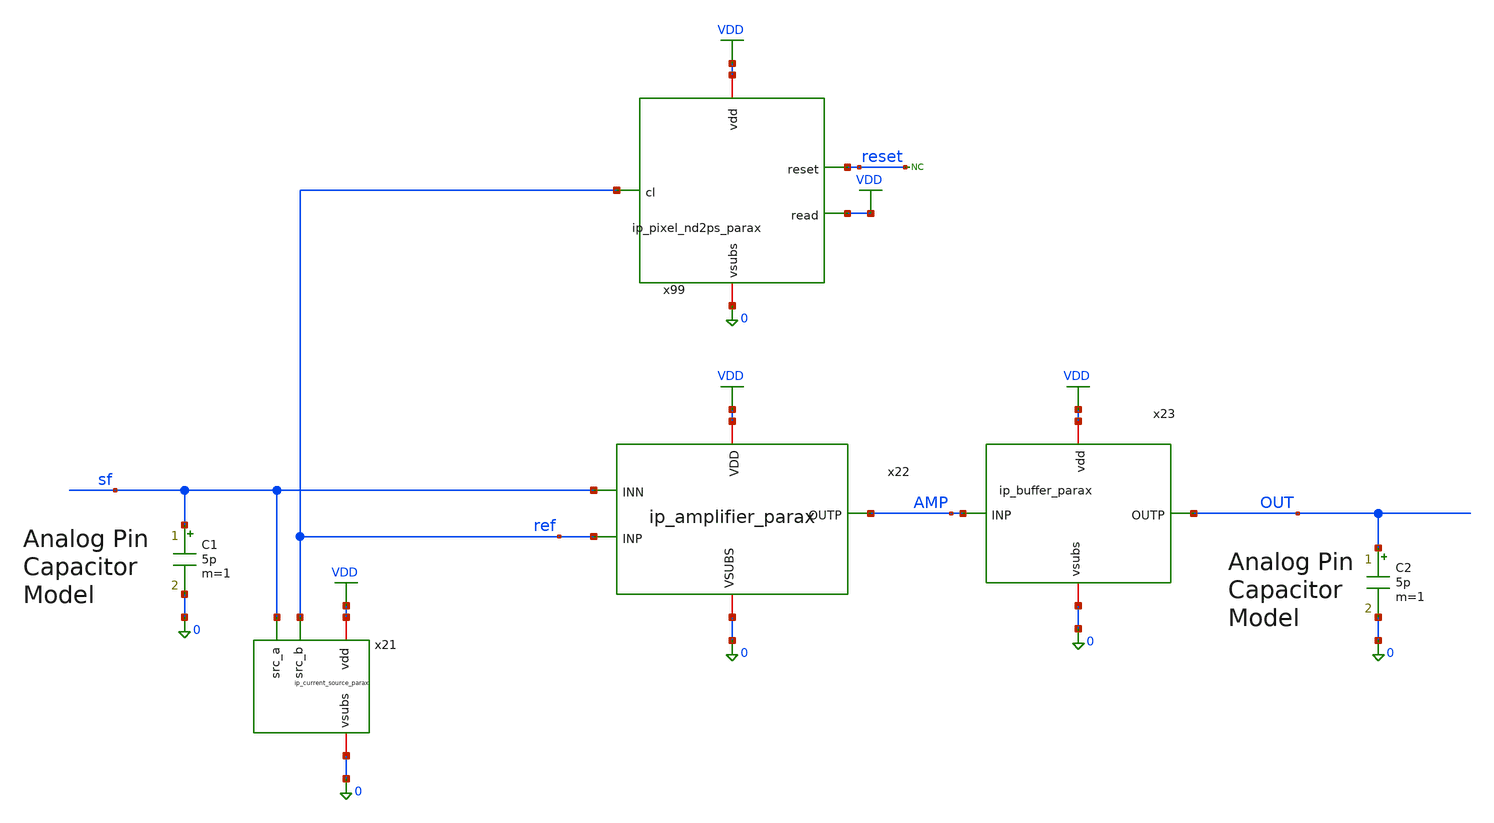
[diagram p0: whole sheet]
** sch_path: xschem/tb_total_tran.sch
**.subckt tb_total_tran
x21 VDD sf 0 ref ip_current_source_parax
x22 VDD AMP ref sf 0 ip_amplifier_parax
x99 VDD reset VDD 0 ref ip_pixel_nd2ps_parax
C1 sf 0 5p m=1
x23 VDD OUT AMP 0 ip_buffer_parax
C2 OUT 0 5p m=1
* noconn reset
**** begin user architecture code

.include $::180MCU_MODELS/design.ngspice
.lib $::180MCU_MODELS/sm141064.ngspice typical
.lib $::180MCU_MODELS/sm141064.ngspice res_typical
.lib $::180MCU_MODELS/sm141064.ngspice moscap_typical
.lib $::180MCU_MODELS/sm141064.ngspice diode_typical




.control
	reset
	tran 1u 1.8m
	save all
	write tb_total_tran.raw
	quit
.endc





VVDD VDD 0 3.3
VCLK CLK 0 PULSE (0 3.3 5u 1n 1n 5u 10u)

astim [RESETA        nRA4 nRA3 nRA2 nRA1 nRA0        nCA4 nCA3 nCA2 nCA1 nCA0] stim
.model stim d_source input_file="../st_total.txt"

acosim[CLK        nCA4 nCA3 nCA2 nCA1 nCA0        nRA4 nRA3 nRA2 nRA1 nRA0        RESETA]
+        [reset        nCY20 nCY19 nCY18 nCY17 nCY16 nCY15        nCY14 nCY13 nCY12 nCY11 nCY10 nCY9         nCY8
+  nCY7  nCY6  nCY5  nCY4  nCY3         nCY2  nCY1  nCY0         nRY16 nRY15 nRY14 nRY13 nRY12 nRY11
+         nRY10 nRY9  nRY8  nRY7  nRY6  nRY5        nRY4  nRY3  nRY2  nRY1  nRY0        ] null dut
.model dut d_cosim simulation="../../verilog/rtl/aux_total_digital/aux_total_digital.so"

RnRA0  nRA0 0 100k
RnRA1  nRA1 0 100k
RnRA2  nRA2 0 100k
RnRA3  nRA3 0 100k
RnRA4  nRA4 0 100k

RnCA0  nCA0 0 100k
RnCA1  nCA1 0 100k
RnCA2  nCA2 0 100k
RnCA3  nCA3 0 100k
RnCA4  nCA4 0 100k

RnRY7  nRY7 0 100k
RnRY6  nRY6 0 100k
RnRY5  nRY5 0 100k
RnRY4  nRY4 0 100k
RnRY3  nRY3 0 100k
RnRY2  nRY2 0 100k
RnRY1  nRY1 0 100k
RnRY0  nRY0 0 100k

RnCY5  nCY5 0 100k
RnCY4  nCY4 0 100k
RnCY3  nCY3 0 100k
RnCY2  nCY2 0 100k
RnCY1  nCY1 0 100k
RnCY0  nCY0 0 100k

Rrsta  reseta 0 100k
Rrst   reset  0 100k

.include pixels.spice


**** end user architecture code
**.ends

* expanding   symbol:  ip_current_source_parax.sym # of pins=4
** sym_path: xschem/ip_current_source.sym
.include [file normalize ./parax/ip_current_source.sim.spice]

* expanding   symbol:  ip_amplifier_parax.sym # of pins=5
** sym_path: xschem/ip_amplifier.sym
.include [file normalize ./parax/ip_amplifier.sim.spice]

* expanding   symbol:  ip_pixel_nd2ps_parax.sym # of pins=5
** sym_path: xschem/ip_pixel_nd2ps.sym
.include [file normalize ./parax/ip_pixel_nd2ps.sim.spice]

* expanding   symbol:  ip_buffer_parax.sym # of pins=4
** sym_path: xschem/ip_buffer.sym
.include [file normalize ./parax/ip_buffer.sim.spice]
.GLOBAL VDD
.end
